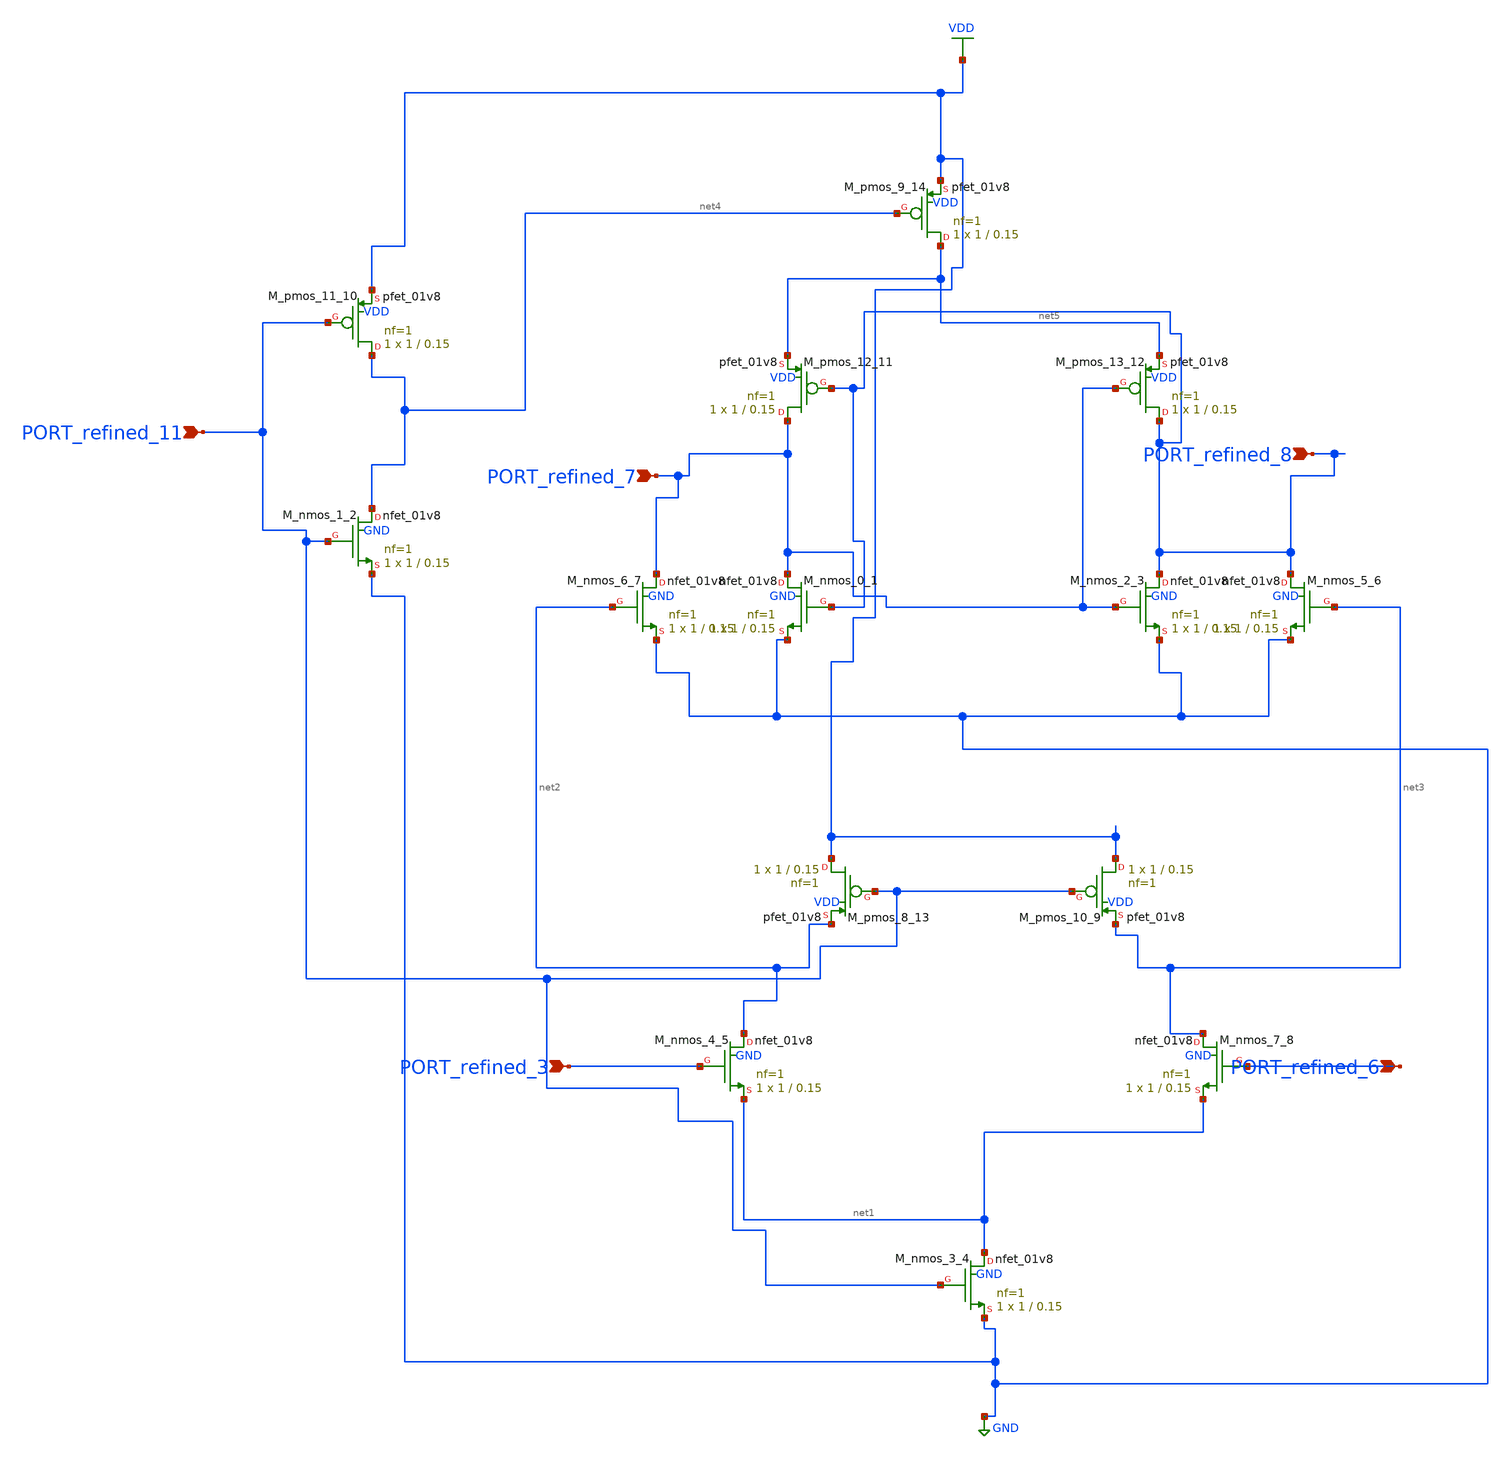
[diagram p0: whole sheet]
** sch_path: schematics/Image2Net/023.sch
**.subckt 023 PORT_refined_8 PORT_refined_7 PORT_refined_6 PORT_refined_11 PORT_refined_3
*.ipin PORT_refined_8
*.ipin PORT_refined_7
*.ipin PORT_refined_6
*.ipin PORT_refined_11
*.ipin PORT_refined_3
XM_nmos_0_1 PORT_refined_7 PORT_refined_8 GND GND sky130_fd_pr__nfet_01v8 L=0.15 W=1 nf=1 ad='int((1 + 1)/2) * 1 / 1 * 0.29'
+ as='int((1 + 2)/2) * 1 / 1 * 0.29' pd='2*int((1 + 1)/2) * (1 / 1 + 0.29)' ps='2*int((1 + 2)/2) * (1 / 1 + 0.29)'
+ nrd='0.29 / 1 ' nrs='0.29 / 1 ' sa=0 sb=0 sd=0 mult=1 m=1
XM_nmos_1_2 net4 PORT_refined_11 GND GND sky130_fd_pr__nfet_01v8 L=0.15 W=1 nf=1 ad='int((1 + 1)/2) * 1 / 1 * 0.29'
+ as='int((1 + 2)/2) * 1 / 1 * 0.29' pd='2*int((1 + 1)/2) * (1 / 1 + 0.29)' ps='2*int((1 + 2)/2) * (1 / 1 + 0.29)'
+ nrd='0.29 / 1 ' nrs='0.29 / 1 ' sa=0 sb=0 sd=0 mult=1 m=1
XM_nmos_2_3 PORT_refined_8 PORT_refined_7 GND GND sky130_fd_pr__nfet_01v8 L=0.15 W=1 nf=1 ad='int((1 + 1)/2) * 1 / 1 * 0.29'
+ as='int((1 + 2)/2) * 1 / 1 * 0.29' pd='2*int((1 + 1)/2) * (1 / 1 + 0.29)' ps='2*int((1 + 2)/2) * (1 / 1 + 0.29)'
+ nrd='0.29 / 1 ' nrs='0.29 / 1 ' sa=0 sb=0 sd=0 mult=1 m=1
XM_nmos_3_4 net1 PORT_refined_11 GND GND sky130_fd_pr__nfet_01v8 L=0.15 W=1 nf=1 ad='int((1 + 1)/2) * 1 / 1 * 0.29'
+ as='int((1 + 2)/2) * 1 / 1 * 0.29' pd='2*int((1 + 1)/2) * (1 / 1 + 0.29)' ps='2*int((1 + 2)/2) * (1 / 1 + 0.29)'
+ nrd='0.29 / 1 ' nrs='0.29 / 1 ' sa=0 sb=0 sd=0 mult=1 m=1
XM_nmos_4_5 net2 PORT_refined_3 net1 GND sky130_fd_pr__nfet_01v8 L=0.15 W=1 nf=1 ad='int((1 + 1)/2) * 1 / 1 * 0.29'
+ as='int((1 + 2)/2) * 1 / 1 * 0.29' pd='2*int((1 + 1)/2) * (1 / 1 + 0.29)' ps='2*int((1 + 2)/2) * (1 / 1 + 0.29)'
+ nrd='0.29 / 1 ' nrs='0.29 / 1 ' sa=0 sb=0 sd=0 mult=1 m=1
XM_nmos_5_6 PORT_refined_8 net3 GND GND sky130_fd_pr__nfet_01v8 L=0.15 W=1 nf=1 ad='int((1 + 1)/2) * 1 / 1 * 0.29'
+ as='int((1 + 2)/2) * 1 / 1 * 0.29' pd='2*int((1 + 1)/2) * (1 / 1 + 0.29)' ps='2*int((1 + 2)/2) * (1 / 1 + 0.29)'
+ nrd='0.29 / 1 ' nrs='0.29 / 1 ' sa=0 sb=0 sd=0 mult=1 m=1
XM_nmos_6_7 PORT_refined_7 net2 GND GND sky130_fd_pr__nfet_01v8 L=0.15 W=1 nf=1 ad='int((1 + 1)/2) * 1 / 1 * 0.29'
+ as='int((1 + 2)/2) * 1 / 1 * 0.29' pd='2*int((1 + 1)/2) * (1 / 1 + 0.29)' ps='2*int((1 + 2)/2) * (1 / 1 + 0.29)'
+ nrd='0.29 / 1 ' nrs='0.29 / 1 ' sa=0 sb=0 sd=0 mult=1 m=1
XM_nmos_7_8 net3 PORT_refined_6 net1 GND sky130_fd_pr__nfet_01v8 L=0.15 W=1 nf=1 ad='int((1 + 1)/2) * 1 / 1 * 0.29'
+ as='int((1 + 2)/2) * 1 / 1 * 0.29' pd='2*int((1 + 1)/2) * (1 / 1 + 0.29)' ps='2*int((1 + 2)/2) * (1 / 1 + 0.29)'
+ nrd='0.29 / 1 ' nrs='0.29 / 1 ' sa=0 sb=0 sd=0 mult=1 m=1
XM_pmos_10_9 VDD PORT_refined_11 net3 VDD sky130_fd_pr__pfet_01v8 L=0.15 W=1 nf=1 ad='int((1 + 1)/2) * 1 / 1 * 0.29'
+ as='int((1 + 2)/2) * 1 / 1 * 0.29' pd='2*int((1 + 1)/2) * (1 / 1 + 0.29)' ps='2*int((1 + 2)/2) * (1 / 1 + 0.29)'
+ nrd='0.29 / 1 ' nrs='0.29 / 1 ' sa=0 sb=0 sd=0 mult=1 m=1
XM_pmos_11_10 net4 PORT_refined_11 VDD VDD sky130_fd_pr__pfet_01v8 L=0.15 W=1 nf=1 ad='int((1 + 1)/2) * 1 / 1 * 0.29'
+ as='int((1 + 2)/2) * 1 / 1 * 0.29' pd='2*int((1 + 1)/2) * (1 / 1 + 0.29)' ps='2*int((1 + 2)/2) * (1 / 1 + 0.29)'
+ nrd='0.29 / 1 ' nrs='0.29 / 1 ' sa=0 sb=0 sd=0 mult=1 m=1
XM_pmos_12_11 PORT_refined_7 PORT_refined_8 net5 VDD sky130_fd_pr__pfet_01v8 L=0.15 W=1 nf=1 ad='int((1 + 1)/2) * 1 / 1 * 0.29'
+ as='int((1 + 2)/2) * 1 / 1 * 0.29' pd='2*int((1 + 1)/2) * (1 / 1 + 0.29)' ps='2*int((1 + 2)/2) * (1 / 1 + 0.29)'
+ nrd='0.29 / 1 ' nrs='0.29 / 1 ' sa=0 sb=0 sd=0 mult=1 m=1
XM_pmos_13_12 PORT_refined_8 PORT_refined_7 net5 VDD sky130_fd_pr__pfet_01v8 L=0.15 W=1 nf=1 ad='int((1 + 1)/2) * 1 / 1 * 0.29'
+ as='int((1 + 2)/2) * 1 / 1 * 0.29' pd='2*int((1 + 1)/2) * (1 / 1 + 0.29)' ps='2*int((1 + 2)/2) * (1 / 1 + 0.29)'
+ nrd='0.29 / 1 ' nrs='0.29 / 1 ' sa=0 sb=0 sd=0 mult=1 m=1
XM_pmos_8_13 VDD PORT_refined_11 net2 VDD sky130_fd_pr__pfet_01v8 L=0.15 W=1 nf=1 ad='int((1 + 1)/2) * 1 / 1 * 0.29'
+ as='int((1 + 2)/2) * 1 / 1 * 0.29' pd='2*int((1 + 1)/2) * (1 / 1 + 0.29)' ps='2*int((1 + 2)/2) * (1 / 1 + 0.29)'
+ nrd='0.29 / 1 ' nrs='0.29 / 1 ' sa=0 sb=0 sd=0 mult=1 m=1
XM_pmos_9_14 net5 net4 VDD VDD sky130_fd_pr__pfet_01v8 L=0.15 W=1 nf=1 ad='int((1 + 1)/2) * 1 / 1 * 0.29'
+ as='int((1 + 2)/2) * 1 / 1 * 0.29' pd='2*int((1 + 1)/2) * (1 / 1 + 0.29)' ps='2*int((1 + 2)/2) * (1 / 1 + 0.29)'
+ nrd='0.29 / 1 ' nrs='0.29 / 1 ' sa=0 sb=0 sd=0 mult=1 m=1
**.ends
.GLOBAL GND
.GLOBAL VDD
.end
